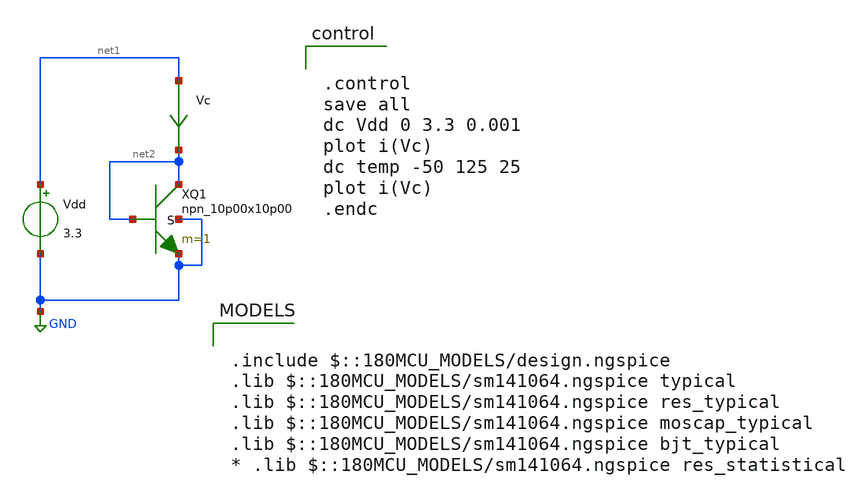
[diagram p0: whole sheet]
** sch_path: npn-diode03v3.sch
**.subckt npn-diode03v3
Vdd net1 GND 3.3
Vc net1 net2 0
.save i(vc)
XQ1 net2 net2 GND GND npn_10p00x10p00 m=1
**** begin user architecture code

.include $::180MCU_MODELS/design.ngspice
.lib $::180MCU_MODELS/sm141064.ngspice typical
.lib $::180MCU_MODELS/sm141064.ngspice res_typical
.lib $::180MCU_MODELS/sm141064.ngspice moscap_typical
.lib $::180MCU_MODELS/sm141064.ngspice bjt_typical
* .lib $::180MCU_MODELS/sm141064.ngspice res_statistical



.control
save all
dc Vdd 0 3.3 0.001
plot i(Vc)
dc temp -50 125 25
plot i(Vc)
.endc


**** end user architecture code
**.ends
.GLOBAL GND
.end
